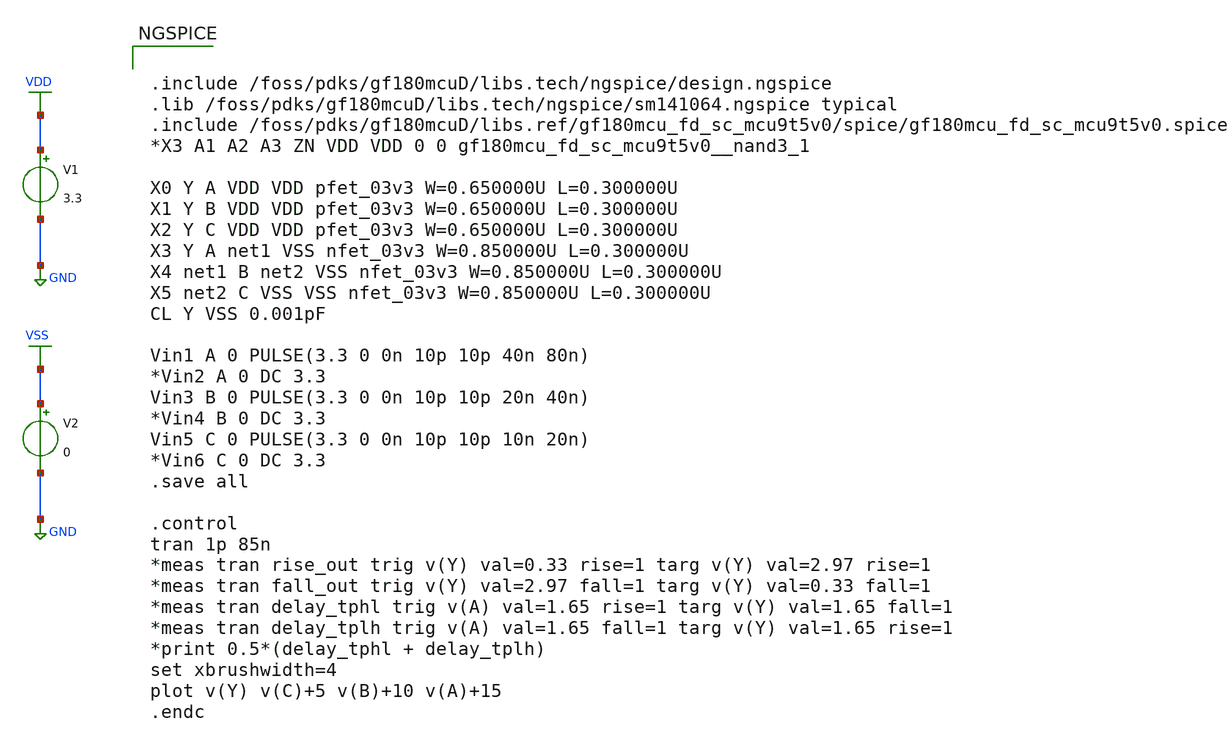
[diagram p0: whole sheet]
** sch_path: designs/libs/tb_NAND3/nand3_test_functional.sch
**.subckt nand3_test_functional
V1 VDD GND 3.3
V2 VSS GND 0
**** begin user architecture code


.include /foss/pdks/gf180mcuD/libs.tech/ngspice/design.ngspice
.lib /foss/pdks/gf180mcuD/libs.tech/ngspice/sm141064.ngspice typical
.include /foss/pdks/gf180mcuD/libs.ref/gf180mcu_fd_sc_mcu9t5v0/spice/gf180mcu_fd_sc_mcu9t5v0.spice
*X3 A1 A2 A3 ZN VDD VDD 0 0 gf180mcu_fd_sc_mcu9t5v0__nand3_1

X0 Y A VDD VDD pfet_03v3 W=0.650000U L=0.300000U
X1 Y B VDD VDD pfet_03v3 W=0.650000U L=0.300000U
X2 Y C VDD VDD pfet_03v3 W=0.650000U L=0.300000U
X3 Y A net1 VSS nfet_03v3 W=0.850000U L=0.300000U
X4 net1 B net2 VSS nfet_03v3 W=0.850000U L=0.300000U
X5 net2 C VSS VSS nfet_03v3 W=0.850000U L=0.300000U
CL Y VSS 0.001pF

Vin1 A 0 PULSE(3.3 0 0n 10p 10p 40n 80n)
*Vin2 A 0 DC 3.3
Vin3 B 0 PULSE(3.3 0 0n 10p 10p 20n 40n)
*Vin4 B 0 DC 3.3
Vin5 C 0 PULSE(3.3 0 0n 10p 10p 10n 20n)
*Vin6 C 0 DC 3.3
.save all

.control
tran 1p 85n
*meas tran rise_out trig v(Y) val=0.33 rise=1 targ v(Y) val=2.97 rise=1
*meas tran fall_out trig v(Y) val=2.97 fall=1 targ v(Y) val=0.33 fall=1
*meas tran delay_tphl trig v(A) val=1.65 rise=1 targ v(Y) val=1.65 fall=1
*meas tran delay_tplh trig v(A) val=1.65 fall=1 targ v(Y) val=1.65 rise=1
*print 0.5*(delay_tphl + delay_tplh)
set xbrushwidth=4
plot v(Y) v(C)+5 v(B)+10 v(A)+15
.endc


**** end user architecture code
**.ends
.GLOBAL VDD
.GLOBAL GND
.GLOBAL VSS
.end
